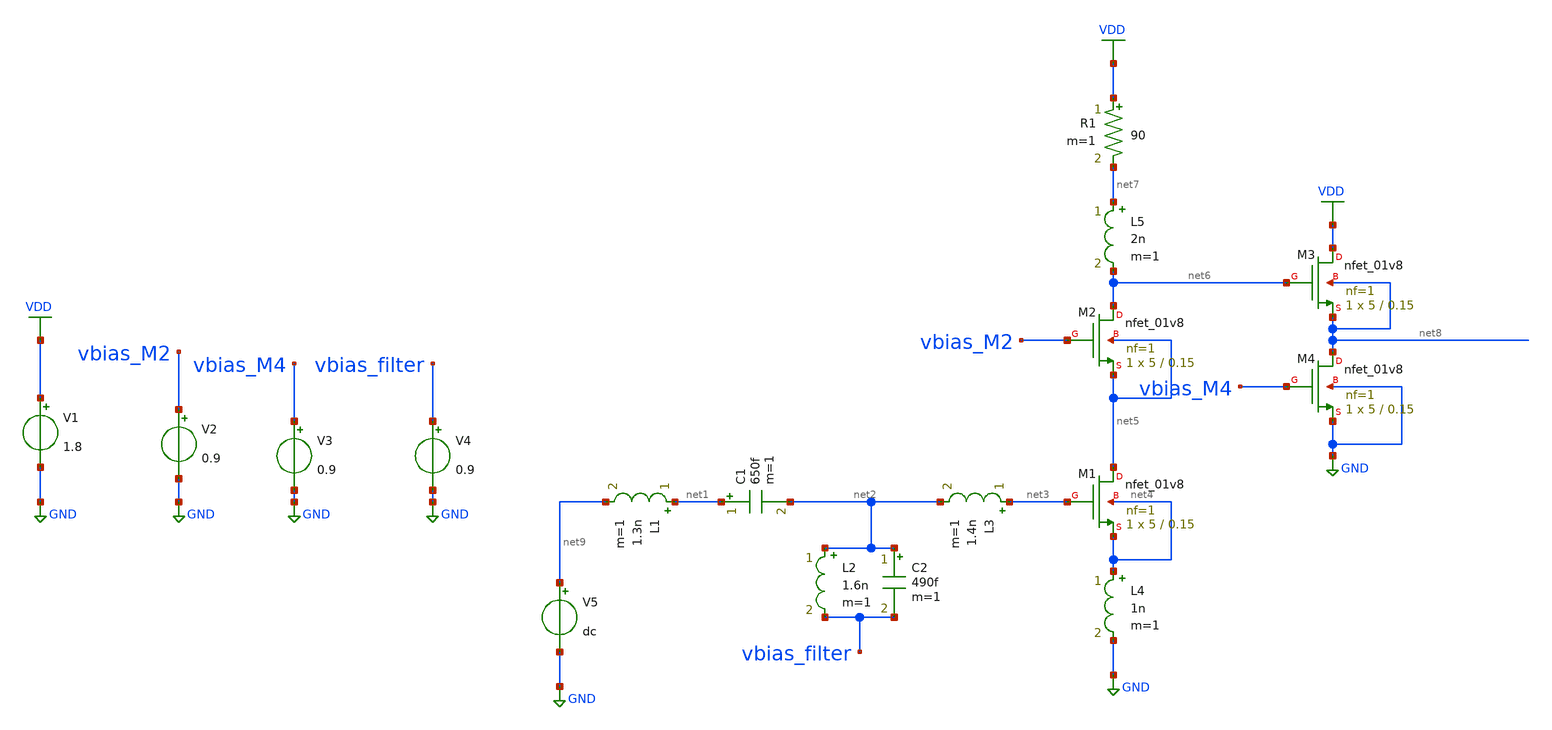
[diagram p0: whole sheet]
** sch_path: nikhil/LNA/LNA.sch
**.subckt LNA
L1 net1 net9 1.3n m=1
L2 net2 vbias_filter 1.6n m=1
L3 net3 net2 1.4n m=1
XM1 net5 net3 net4 net4 sky130_fd_pr__nfet_01v8 L=0.15 W=5 nf=1 ad='int((nf+1)/2) * W/nf * 0.29' as='int((nf+2)/2) * W/nf * 0.29'
+ pd='2*int((nf+1)/2) * (W/nf + 0.29)' ps='2*int((nf+2)/2) * (W/nf + 0.29)' nrd='0.29 / W' nrs='0.29 / W'
+ sa=0 sb=0 sd=0 mult=1 m=1
L4 net4 GND 1n m=1
XM2 net6 vbias_M2 net5 net5 sky130_fd_pr__nfet_01v8 L=0.15 W=5 nf=1 ad='int((nf+1)/2) * W/nf * 0.29'
+ as='int((nf+2)/2) * W/nf * 0.29' pd='2*int((nf+1)/2) * (W/nf + 0.29)' ps='2*int((nf+2)/2) * (W/nf + 0.29)'
+ nrd='0.29 / W' nrs='0.29 / W' sa=0 sb=0 sd=0 mult=1 m=1
L5 net7 net6 2n m=1
R1 VDD net7 90 m=1
XM3 VDD net6 net8 net8 sky130_fd_pr__nfet_01v8 L=0.15 W=5 nf=1 ad='int((nf+1)/2) * W/nf * 0.29' as='int((nf+2)/2) * W/nf * 0.29'
+ pd='2*int((nf+1)/2) * (W/nf + 0.29)' ps='2*int((nf+2)/2) * (W/nf + 0.29)' nrd='0.29 / W' nrs='0.29 / W'
+ sa=0 sb=0 sd=0 mult=1 m=1
XM4 net8 vbias_M4 GND GND sky130_fd_pr__nfet_01v8 L=0.15 W=5 nf=1 ad='int((nf+1)/2) * W/nf * 0.29' as='int((nf+2)/2) * W/nf * 0.29'
+ pd='2*int((nf+1)/2) * (W/nf + 0.29)' ps='2*int((nf+2)/2) * (W/nf + 0.29)' nrd='0.29 / W' nrs='0.29 / W'
+ sa=0 sb=0 sd=0 mult=1 m=1
V1 VDD GND 1.8
V2 vbias_M2 GND 0.9
V3 vbias_M4 GND 0.9
V4 vbias_filter GND 0.9
C1 net1 net2 650f m=1
C2 net2 vbias_filter 490f m=1
V5 net9 GND dc
**** begin user architecture code

.options wnflag=1
.include /pdk/open_pdks/sources/sky130-pdk/libraries/sky130_fd_pr/latest/cells/nfet_01v8/sky130_fd_pr__nfet_01v8__tt.corner.spice
.include /pdk/open_pdks/sources/sky130-pdk/libraries/sky130_fd_pr/latest/cells/nfet_01v8_lvt/sky130_fd_pr__nfet_01v8_lvt__tt.corner.spice
.include /pdk/open_pdks/sources/sky130-pdk/libraries/sky130_fd_pr/latest/cells/pfet_01v8/sky130_fd_pr__pfet_01v8__tt.corner.spice
.include /pdk/open_pdks/sources/sky130-pdk/libraries/sky130_fd_pr/latest/cells/nfet_03v3_nvt/sky130_fd_pr__nfet_03v3_nvt__tt.corner.spice
.include /pdk/open_pdks/sources/sky130-pdk/libraries/sky130_fd_pr/latest/cells/nfet_05v0_nvt/sky130_fd_pr__nfet_05v0_nvt__tt.corner.spice
.include /pdk/open_pdks/sources/sky130-pdk/libraries/sky130_fd_pr/latest/cells/esd_nfet_01v8/sky130_fd_pr__esd_nfet_01v8__tt.corner.spice
.include /pdk/open_pdks/sources/sky130-pdk/libraries/sky130_fd_pr/latest/cells/pfet_01v8_lvt/sky130_fd_pr__pfet_01v8_lvt__tt.corner.spice
.include /pdk/open_pdks/sources/sky130-pdk/libraries/sky130_fd_pr/latest/cells/pfet_01v8_hvt/sky130_fd_pr__pfet_01v8_hvt__tt.corner.spice
.include /pdk/open_pdks/sources/sky130-pdk/libraries/sky130_fd_pr/latest/cells/esd_pfet_g5v0d10v5/sky130_fd_pr__esd_pfet_g5v0d10v5__tt.corner.spice
.include /pdk/open_pdks/sources/sky130-pdk/libraries/sky130_fd_pr/latest/cells/pfet_g5v0d10v5/sky130_fd_pr__pfet_g5v0d10v5__tt.corner.spice
.include /pdk/open_pdks/sources/sky130-pdk/libraries/sky130_fd_pr/latest/cells/pfet_g5v0d16v0/sky130_fd_pr__pfet_g5v0d16v0__tt.corner.spice
.include /pdk/open_pdks/sources/sky130-pdk/libraries/sky130_fd_pr/latest/cells/nfet_g5v0d10v5/sky130_fd_pr__nfet_g5v0d10v5__tt.corner.spice
.include /pdk/open_pdks/sources/sky130-pdk/libraries/sky130_fd_pr/latest/cells/nfet_g5v0d16v0/sky130_fd_pr__nfet_g5v0d16v0__tt_discrete.corner.spice
.include /pdk/open_pdks/sources/sky130-pdk/libraries/sky130_fd_pr/latest/cells/esd_nfet_g5v0d10v5/sky130_fd_pr__esd_nfet_g5v0d10v5__tt.corner.spice
.include /pdk/open_pdks/sources/sky130-pdk/libraries/sky130_fd_pr/latest/models/corners/tt/nonfet.spice
* Mismatch parameters
.include /pdk/open_pdks/sources/sky130-pdk/libraries/sky130_fd_pr/latest/cells/nfet_01v8/sky130_fd_pr__nfet_01v8__mismatch.corner.spice
.include /pdk/open_pdks/sources/sky130-pdk/libraries/sky130_fd_pr/latest/cells/pfet_01v8/sky130_fd_pr__pfet_01v8__mismatch.corner.spice
.include /pdk/open_pdks/sources/sky130-pdk/libraries/sky130_fd_pr/latest/cells/nfet_01v8_lvt/sky130_fd_pr__nfet_01v8_lvt__mismatch.corner.spice
.include /pdk/open_pdks/sources/sky130-pdk/libraries/sky130_fd_pr/latest/cells/pfet_01v8_lvt/sky130_fd_pr__pfet_01v8_lvt__mismatch.corner.spice
.include /pdk/open_pdks/sources/sky130-pdk/libraries/sky130_fd_pr/latest/cells/pfet_01v8_hvt/sky130_fd_pr__pfet_01v8_hvt__mismatch.corner.spice
.include /pdk/open_pdks/sources/sky130-pdk/libraries/sky130_fd_pr/latest/cells/nfet_g5v0d10v5/sky130_fd_pr__nfet_g5v0d10v5__mismatch.corner.spice
.include /pdk/open_pdks/sources/sky130-pdk/libraries/sky130_fd_pr/latest/cells/pfet_g5v0d10v5/sky130_fd_pr__pfet_g5v0d10v5__mismatch.corner.spice
.include /pdk/open_pdks/sources/sky130-pdk/libraries/sky130_fd_pr/latest/cells/nfet_05v0_nvt/sky130_fd_pr__nfet_05v0_nvt__mismatch.corner.spice
.include /pdk/open_pdks/sources/sky130-pdk/libraries/sky130_fd_pr/latest/cells/nfet_03v3_nvt/sky130_fd_pr__nfet_03v3_nvt__mismatch.corner.spice
* Resistor$::SKYWATER_MODELS/Capacitor
.include /pdk/open_pdks/sources/sky130-pdk/libraries/sky130_fd_pr/latest/models/r+c/res_typical__cap_typical.spice
.include /pdk/open_pdks/sources/sky130-pdk/libraries/sky130_fd_pr/latest/models/r+c/res_typical__cap_typical__lin.spice
* Special cells
.include /pdk/open_pdks/sources/sky130-pdk/libraries/sky130_fd_pr/latest/models/corners/tt/specialized_cells.spice
* All models
.include /pdk/open_pdks/sources/sky130-pdk/libraries/sky130_fd_pr/latest/models/all.spice
* Corner
.include /pdk/open_pdks/sources/sky130-pdk/libraries/sky130_fd_pr/latest/models/corners/tt/rf.spice


.ac

**** end user architecture code
**.ends
.GLOBAL GND
.GLOBAL VDD
.end
